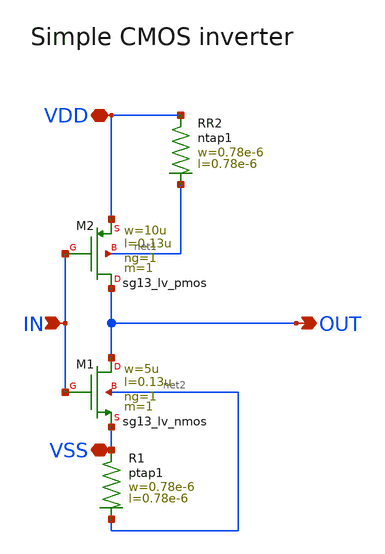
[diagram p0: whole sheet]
** sch_path: schematics/xinv.sch
**.subckt xinv VSS VDD OUT IN
*.iopin VSS
*.iopin VDD
*.opin OUT
*.ipin IN
XM1 OUT IN VSS net2 sg13_lv_nmos w=5u l=0.13u ng=1 m=1 mm_ok=1
XM2 OUT IN VDD net1 sg13_lv_pmos w=10u l=0.13u ng=1 m=1 mm_ok=1
XR1 VSS net2 ptap1 R=262.8 w=0.78e-6 l=0.78e-6
XR2 VDD net1 ntap1 R=262.8 w=0.78e-6 l=0.78e-6
**.ends
.end
